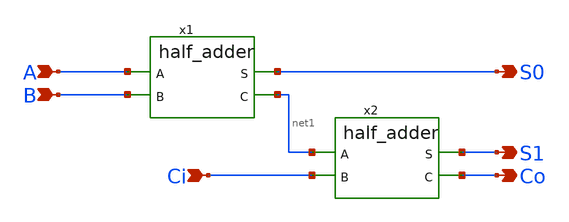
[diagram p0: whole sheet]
** sch_path: circuits/xschem/full_adder.sch
**.subckt full_adder A B Ci S0 S1 Co
*.ipin A
*.ipin B
*.ipin Ci
*.opin S0
*.opin S1
*.opin Co
x1 A S0 B net1 half_adder
x2 net1 S1 Ci Co half_adder
**.ends
.end
